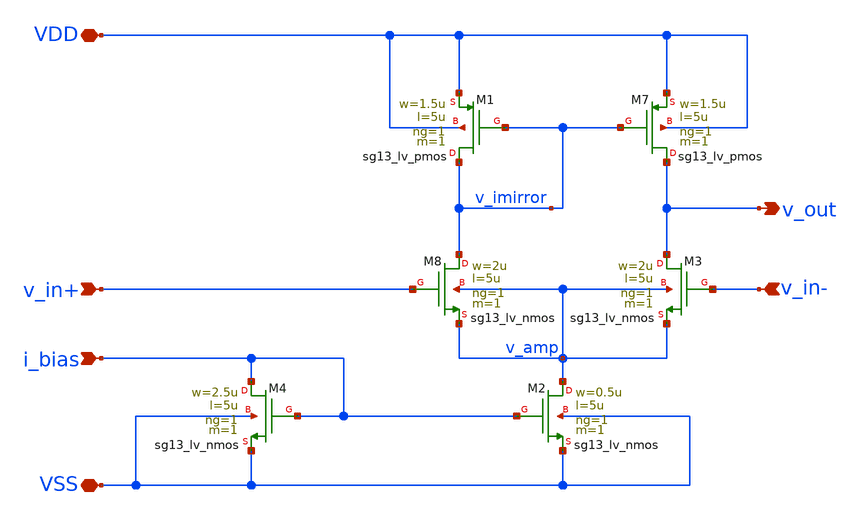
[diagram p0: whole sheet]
** sch_path: 3_Real_Cir/10_Real_Cir/self_build_opamp.sch
**.subckt self_build_opamp v_in+ v_in- v_out VDD VSS i_bias
*.ipin v_in+
*.ipin v_in-
*.opin v_out
*.iopin VDD
*.iopin VSS
*.ipin i_bias
XM7 v_out v_imirror VDD VDD sg13_lv_pmos w=1.5u l=5u ng=1 m=1 mm_ok=1
XM1 v_imirror v_imirror VDD VDD sg13_lv_pmos w=1.5u l=5u ng=1 m=1 mm_ok=1
XM8 v_imirror v_in+ v_amp v_amp sg13_lv_nmos w=2u l=5u ng=1 m=1 mm_ok=1
XM3 v_out v_in- v_amp v_amp sg13_lv_nmos w=2u l=5u ng=1 m=1 mm_ok=1
XM2 v_amp i_bias VSS VSS sg13_lv_nmos w=0.5u l=5u ng=1 m=1 mm_ok=1
XM4 i_bias i_bias VSS VSS sg13_lv_nmos w=2.5u l=5u ng=1 m=1 mm_ok=1
**.ends
.end
